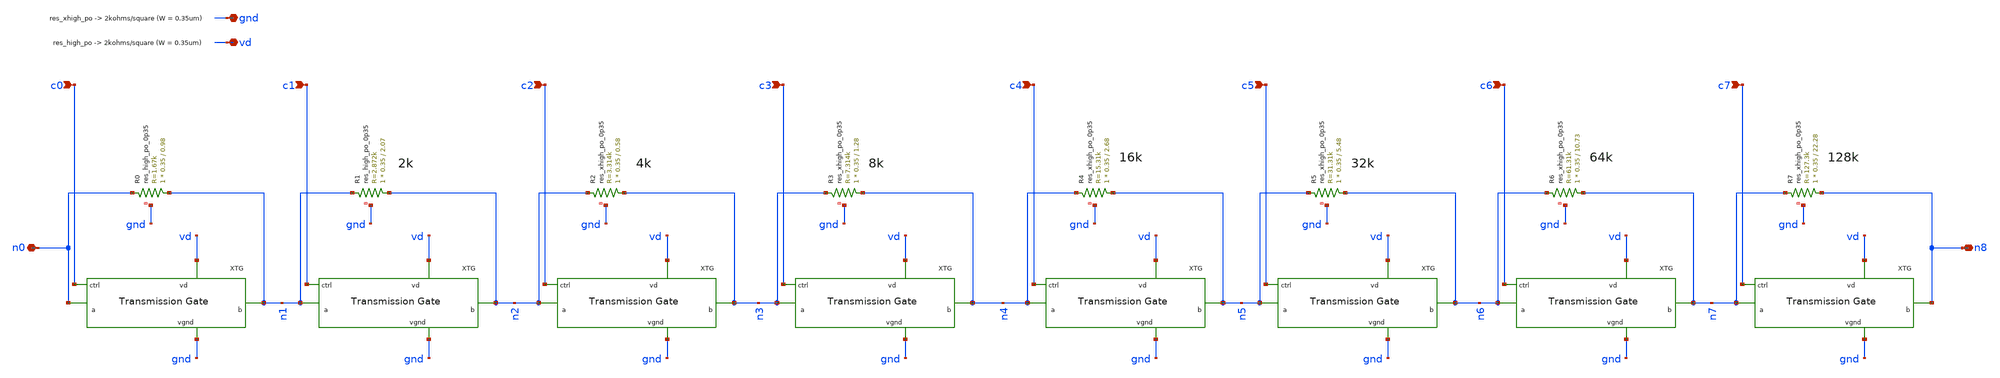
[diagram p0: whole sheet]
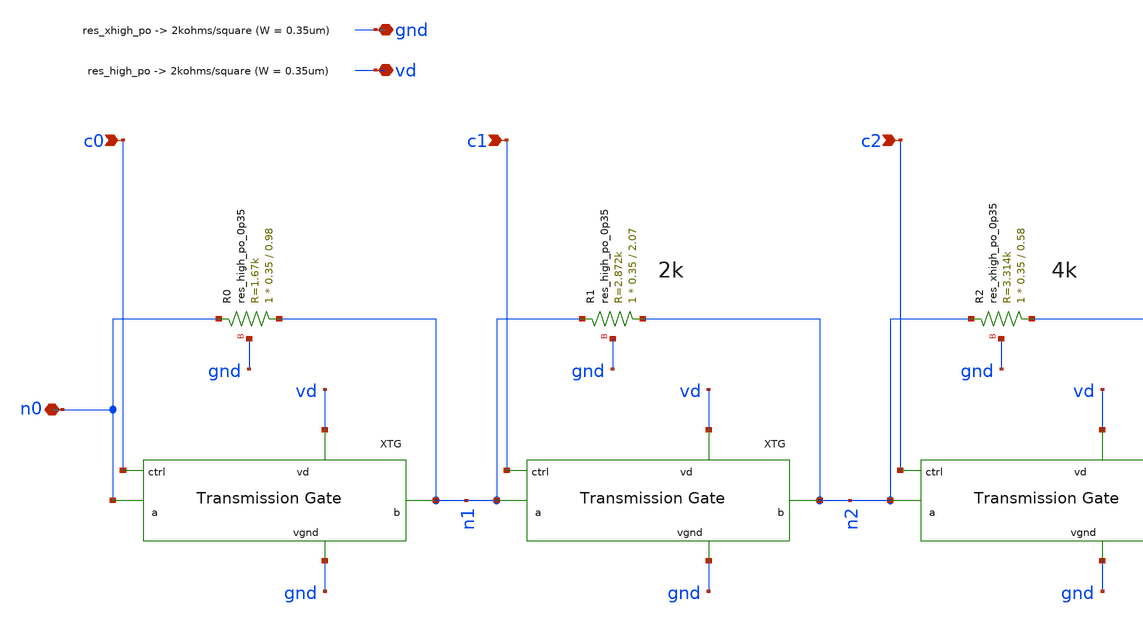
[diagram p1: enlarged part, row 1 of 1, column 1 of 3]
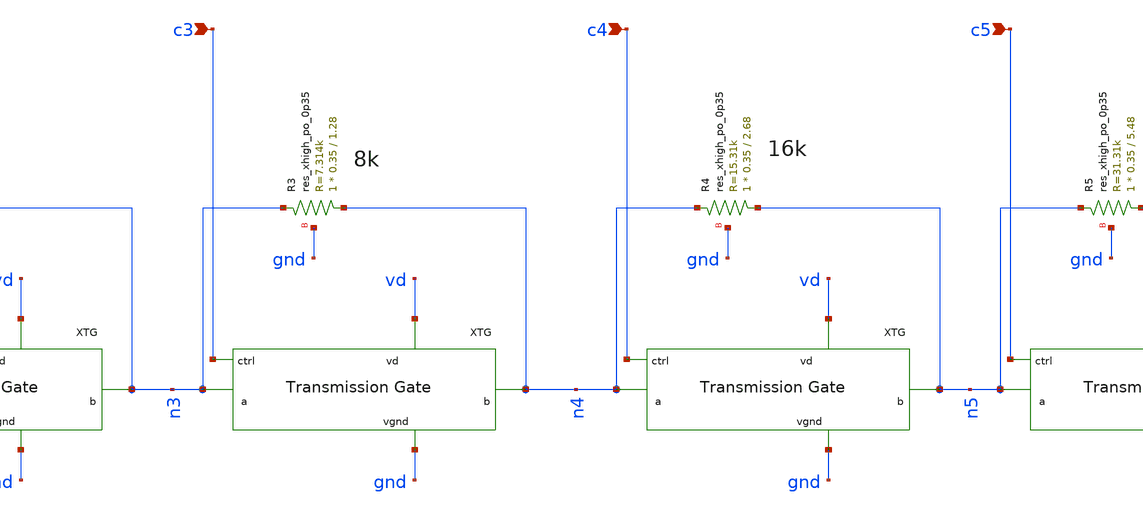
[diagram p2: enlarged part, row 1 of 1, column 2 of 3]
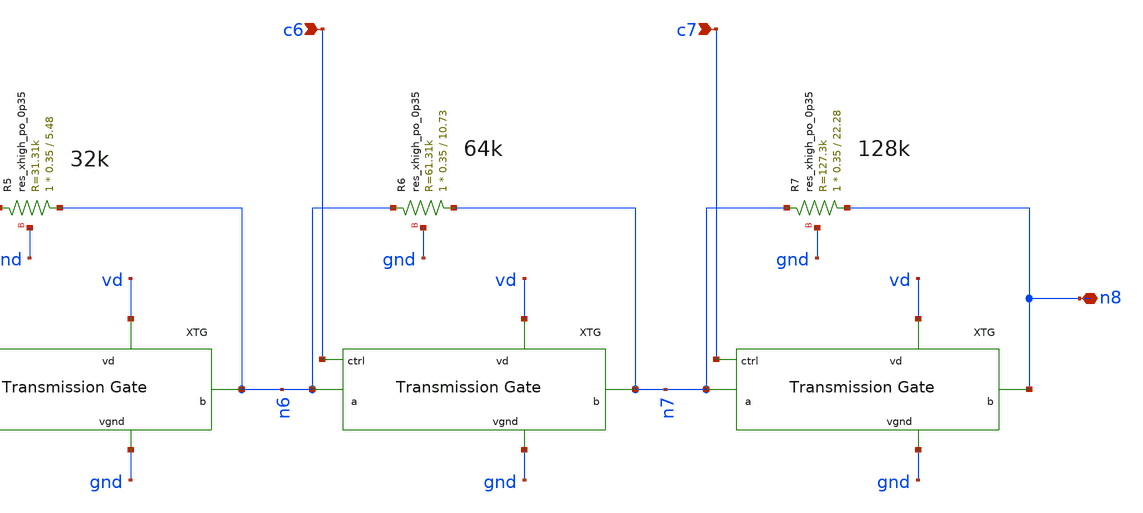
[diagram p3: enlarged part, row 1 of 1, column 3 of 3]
** sch_path: xschem/digpot.sch
**.subckt digpot c0 c1 c2 c3 c4 c5 c6 c7 gnd vd n0 n8
*.ipin c0
*.ipin c1
*.ipin c2
*.ipin c3
*.ipin c4
*.ipin c5
*.ipin c6
*.ipin c7
*.iopin gnd
*.iopin vd
*.iopin n0
*.iopin n8
xtg1 c0 vd n1 gnd n0 tg
xtg2 c1 vd n2 gnd n1 tg
xtg3 c2 vd n3 gnd n2 tg
xtg4 c3 vd n4 gnd n3 tg
xtg5 c4 vd n5 gnd n4 tg
xtg6 c5 vd n6 gnd n5 tg
xtg7 c6 vd n7 gnd n6 tg
xtg8 c7 vd n8 gnd n7 tg
XR0 n1 n0 gnd sky130_fd_pr__res_high_po_0p35 L=0.98 mult=1 m=1
XR1 n2 n1 gnd sky130_fd_pr__res_high_po_0p35 L=2.07 mult=1 m=1
XR2 n3 n2 gnd sky130_fd_pr__res_xhigh_po_0p35 L=0.58 mult=1 m=1
XR3 n4 n3 gnd sky130_fd_pr__res_xhigh_po_0p35 L=1.28 mult=1 m=1
XR4 n5 n4 gnd sky130_fd_pr__res_xhigh_po_0p35 L=2.68 mult=1 m=1
XR5 n6 n5 gnd sky130_fd_pr__res_xhigh_po_0p35 L=5.48 mult=1 m=1
XR6 n7 n6 gnd sky130_fd_pr__res_xhigh_po_0p35 L=10.73 mult=1 m=1
XR7 n8 n7 gnd sky130_fd_pr__res_xhigh_po_0p35 L=22.28 mult=1 m=1
**.ends

* expanding   symbol:  /home/hugodg/sky130_skel/dpga-ieee-sscs-contest-main/xschem/tg.sym # of
*+ pins=5
** sym_path: xschem/tg.sym
** sch_path: xschem/tg.sch
.subckt tg ctrl vd b vgnd a
*.iopin vd
*.iopin vgnd
*.iopin b
*.iopin a
*.ipin ctrl
XM2 a ctrl b b sky130_fd_pr__pfet_01v8 L=0.15 W=3 nf=1 ad='int((nf+1)/2) * W/nf * 0.29' as='int((nf+2)/2) * W/nf * 0.29'
+ pd='2*int((nf+1)/2) * (W/nf + 0.29)' ps='2*int((nf+2)/2) * (W/nf + 0.29)' nrd='0.29 / W' nrs='0.29 / W'
+ sa=0 sb=0 sd=0 mult=1 m=1
XM1 b nctrl net1 net1 sky130_fd_pr__nfet_01v8 L=0.15 W=1 nf=1 ad='int((nf+1)/2) * W/nf * 0.29' as='int((nf+2)/2) * W/nf * 0.29'
+ pd='2*int((nf+1)/2) * (W/nf + 0.29)' ps='2*int((nf+2)/2) * (W/nf + 0.29)' nrd='0.29 / W' nrs='0.29 / W'
+ sa=0 sb=0 sd=0 mult=1 m=1
XM3 nctrl ctrl vgnd vgnd sky130_fd_pr__nfet_01v8 L=0.15 W=1 nf=1 ad='int((nf+1)/2) * W/nf * 0.29' as='int((nf+2)/2) * W/nf * 0.29'
+ pd='2*int((nf+1)/2) * (W/nf + 0.29)' ps='2*int((nf+2)/2) * (W/nf + 0.29)' nrd='0.29 / W' nrs='0.29 / W'
+ sa=0 sb=0 sd=0 mult=1 m=1
XM4 nctrl ctrl vd vd sky130_fd_pr__pfet_01v8 L=0.15 W=3 nf=1 ad='int((nf+1)/2) * W/nf * 0.29' as='int((nf+2)/2) * W/nf * 0.29'
+ pd='2*int((nf+1)/2) * (W/nf + 0.29)' ps='2*int((nf+2)/2) * (W/nf + 0.29)' nrd='0.29 / W' nrs='0.29 / W'
+ sa=0 sb=0 sd=0 mult=1 m=1
.ends

.end
